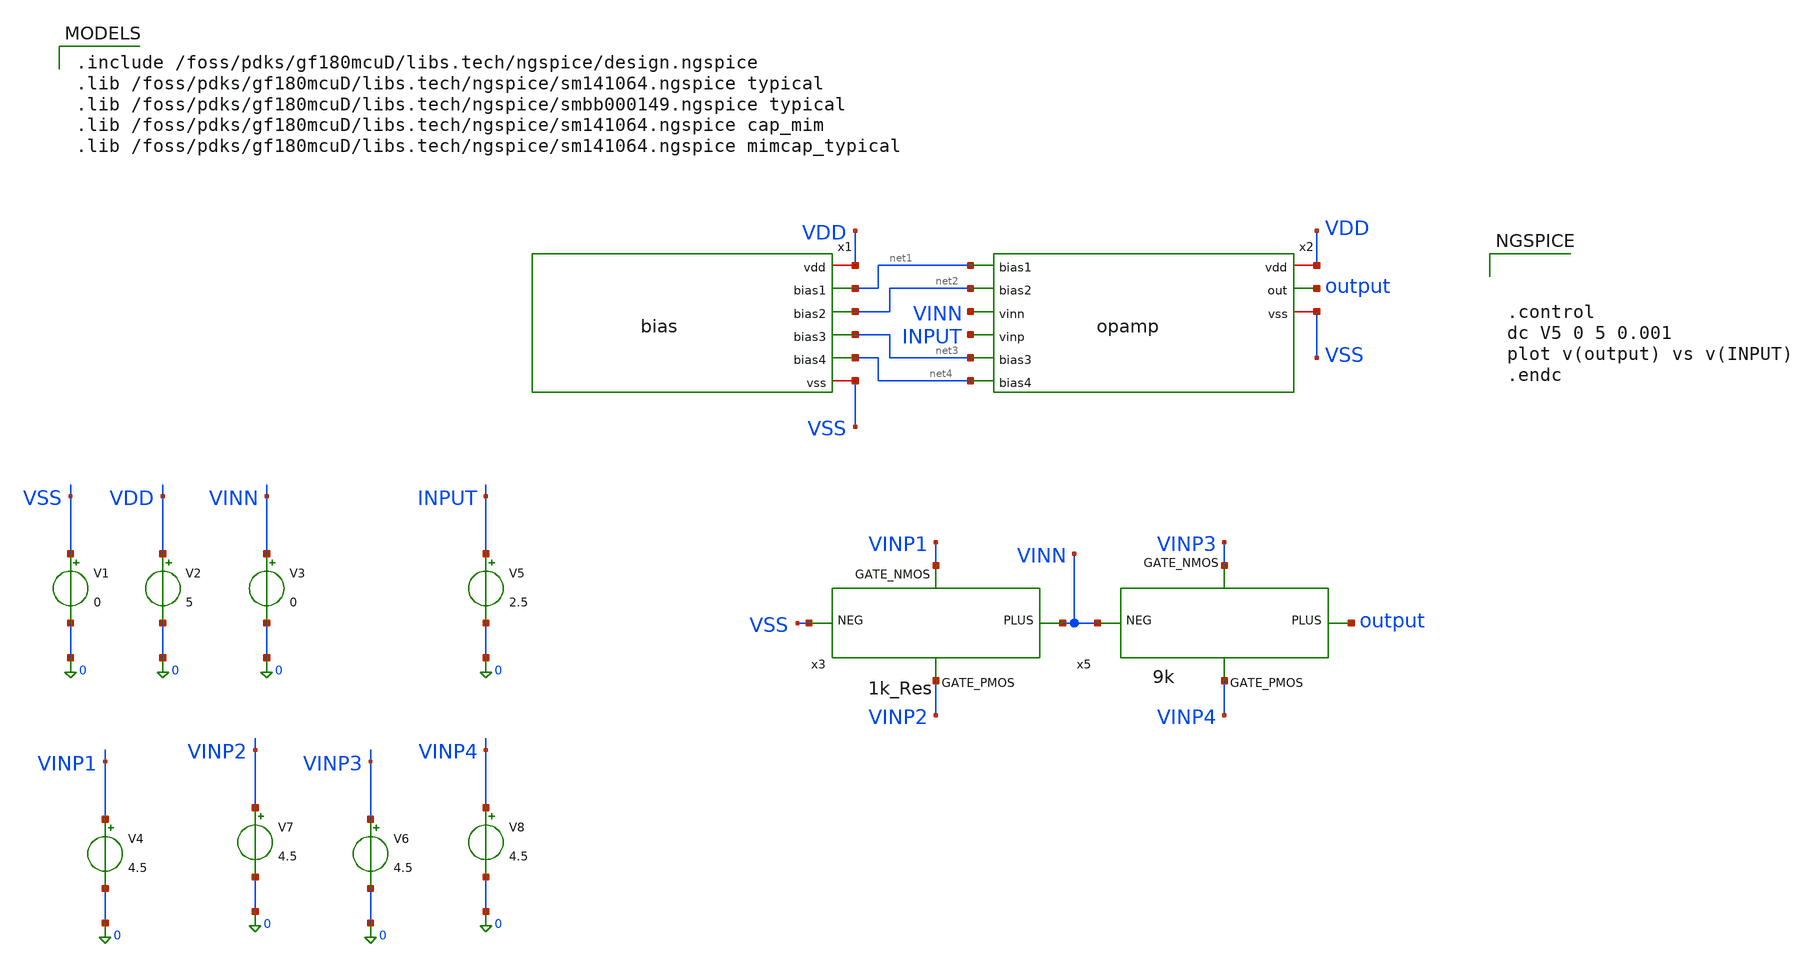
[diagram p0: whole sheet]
** sch_path: activities/opamp3AKAM/simulations_testbench/10kGain.sch
**.subckt 10kGain
x1 VDD net1 net2 net3 net4 VSS bias
x2 VDD net1 net2 VINN output INPUT net3 net4 VSS opamp
V1 VSS 0 0
V2 VDD 0 5
V3 VINN 0 0
V4 VINP1 0 4.5
V5 INPUT 0 2.5
x5 output VINP4 VINP3 VINN 9k
x3 VINN VINP2 VINP1 VSS 1k
V6 VINP3 0 4.5
V7 VINP2 0 4.5
V8 VINP4 0 4.5
**** begin user architecture code



.control
dc V5 0 5 0.001
plot v(output) vs v(INPUT)
.endc



.include /foss/pdks/gf180mcuD/libs.tech/ngspice/design.ngspice
.lib /foss/pdks/gf180mcuD/libs.tech/ngspice/sm141064.ngspice typical
.lib /foss/pdks/gf180mcuD/libs.tech/ngspice/smbb000149.ngspice typical
.lib /foss/pdks/gf180mcuD/libs.tech/ngspice/sm141064.ngspice cap_mim
.lib /foss/pdks/gf180mcuD/libs.tech/ngspice/sm141064.ngspice mimcap_typical

**** end user architecture code
**.ends
.end
